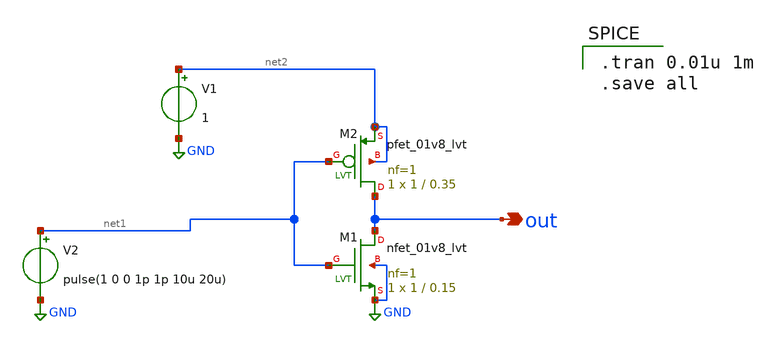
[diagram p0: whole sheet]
** sch_path: component/Reduntant_Inverter/lvt_test.sch
**.subckt lvt_test out
*.opin out
XM2 out net1 net2 net2 sky130_fd_pr__pfet_01v8_lvt L=0.35 W=1 nf=1 ad='int((nf+1)/2) * W/nf * 0.29' as='int((nf+2)/2) * W/nf * 0.29'
+ pd='2*int((nf+1)/2) * (W/nf + 0.29)' ps='2*int((nf+2)/2) * (W/nf + 0.29)' nrd='0.29 / W' nrs='0.29 / W'
+ sa=0 sb=0 sd=0 mult=1 m=1
XM1 out net1 GND GND sky130_fd_pr__nfet_01v8_lvt L=0.15 W=1 nf=1 ad='int((nf+1)/2) * W/nf * 0.29' as='int((nf+2)/2) * W/nf * 0.29'
+ pd='2*int((nf+1)/2) * (W/nf + 0.29)' ps='2*int((nf+2)/2) * (W/nf + 0.29)' nrd='0.29 / W' nrs='0.29 / W'
+ sa=0 sb=0 sd=0 mult=1 m=1
V1 net2 GND 1
V2 net1 GND pulse(1 0 0 1p 1p 10u 20u)
**** begin user architecture code

** opencircuitdesign pdks install
.lib $::SKYWATER_MODELS/sky130.lib.spice tt



.tran 0.01u 1m
.save all

**** end user architecture code
**.ends
.GLOBAL GND
.end
